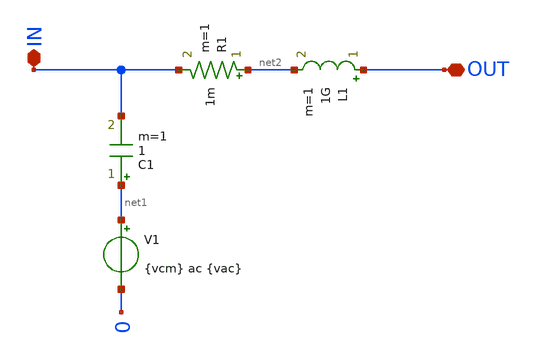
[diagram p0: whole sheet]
** sch_path: schema/ac_probe/ac_probe.sch
**.subckt ac_probe IN OUT
*.iopin IN
*.iopin OUT
C1 net1 IN 1 m=1
V1 net1 0 {vcm} ac {vac}
L1 OUT net2 1G m=1
R1 net2 IN 1m m=1
**.ends
.end
